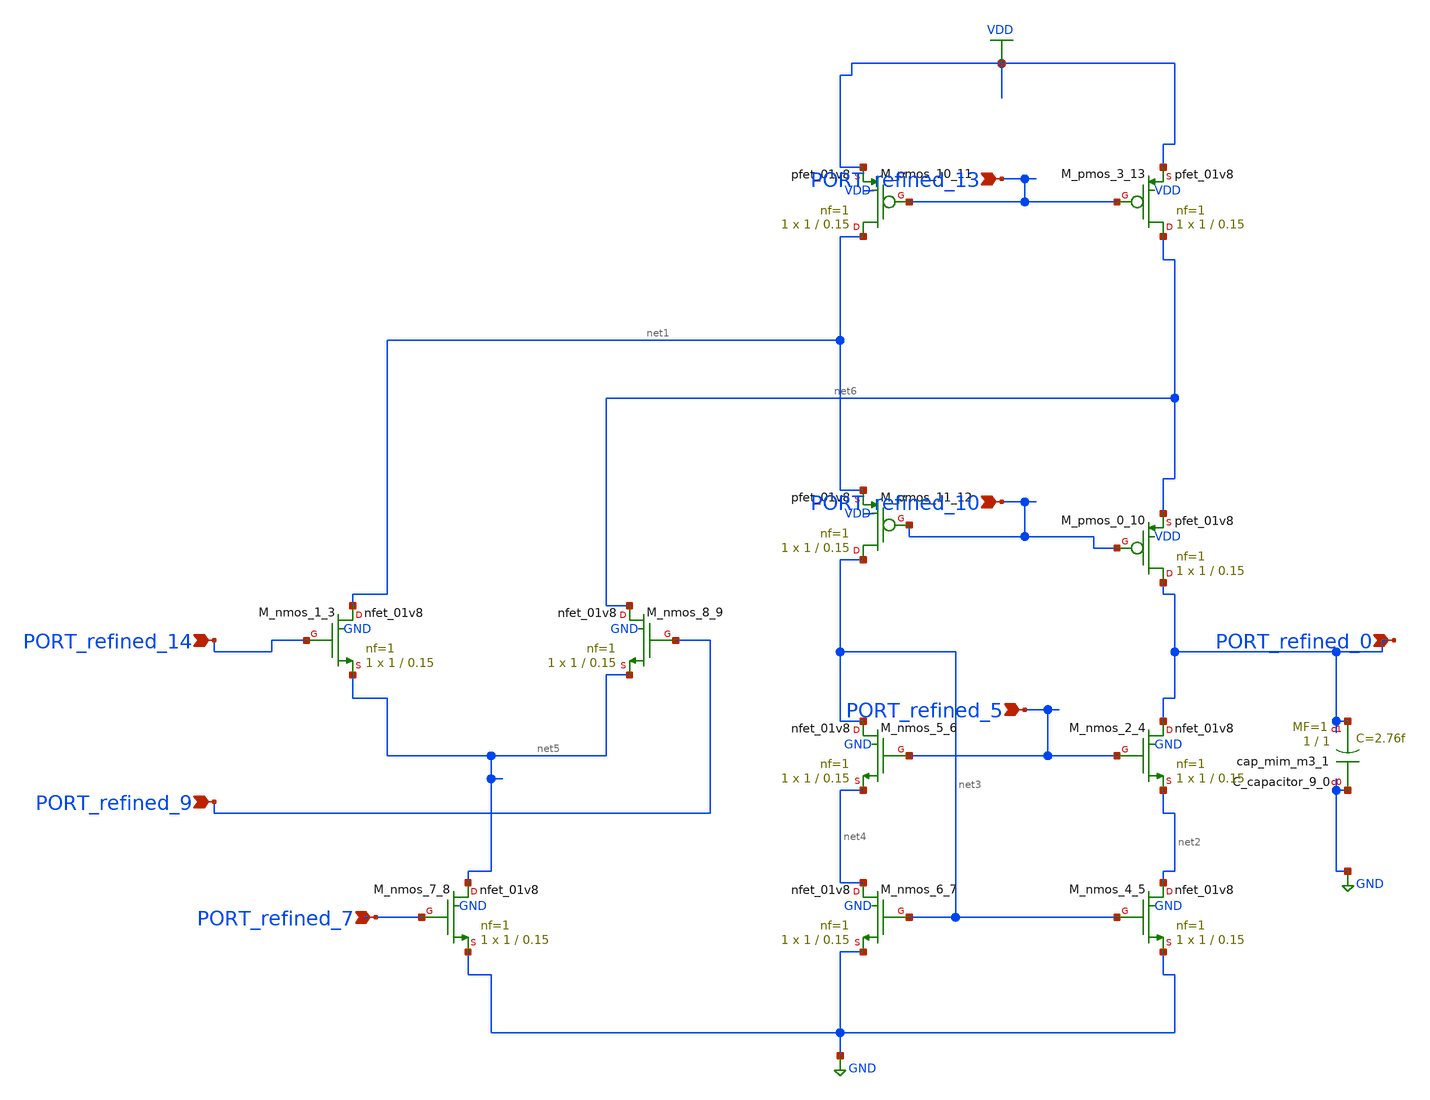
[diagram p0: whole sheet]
** sch_path: schematics/Image2Net/111.sch
**.subckt 111 PORT_refined_14 PORT_refined_0 PORT_refined_9 PORT_refined_7 PORT_refined_10
*+ PORT_refined_13 PORT_refined_5
*.ipin PORT_refined_14
*.ipin PORT_refined_0
*.ipin PORT_refined_9
*.ipin PORT_refined_7
*.ipin PORT_refined_10
*.ipin PORT_refined_13
*.ipin PORT_refined_5
XC_capacitor_9_0 GND PORT_refined_0 sky130_fd_pr__cap_mim_m3_1 W=1 L=1 MF=1 m=1
XM_nmos_1_3 net1 PORT_refined_14 net5 GND sky130_fd_pr__nfet_01v8 L=0.15 W=1 nf=1 ad='int((1 + 1)/2) * 1 / 1 * 0.29'
+ as='int((1 + 2)/2) * 1 / 1 * 0.29' pd='2*int((1 + 1)/2) * (1 / 1 + 0.29)' ps='2*int((1 + 2)/2) * (1 / 1 + 0.29)'
+ nrd='0.29 / 1 ' nrs='0.29 / 1 ' sa=0 sb=0 sd=0 mult=1 m=1
XM_nmos_2_4 PORT_refined_0 PORT_refined_5 net2 GND sky130_fd_pr__nfet_01v8 L=0.15 W=1 nf=1 ad='int((1 + 1)/2) * 1 / 1 * 0.29'
+ as='int((1 + 2)/2) * 1 / 1 * 0.29' pd='2*int((1 + 1)/2) * (1 / 1 + 0.29)' ps='2*int((1 + 2)/2) * (1 / 1 + 0.29)'
+ nrd='0.29 / 1 ' nrs='0.29 / 1 ' sa=0 sb=0 sd=0 mult=1 m=1
XM_nmos_4_5 net2 net3 GND GND sky130_fd_pr__nfet_01v8 L=0.15 W=1 nf=1 ad='int((1 + 1)/2) * 1 / 1 * 0.29'
+ as='int((1 + 2)/2) * 1 / 1 * 0.29' pd='2*int((1 + 1)/2) * (1 / 1 + 0.29)' ps='2*int((1 + 2)/2) * (1 / 1 + 0.29)'
+ nrd='0.29 / 1 ' nrs='0.29 / 1 ' sa=0 sb=0 sd=0 mult=1 m=1
XM_nmos_5_6 net3 PORT_refined_5 net4 GND sky130_fd_pr__nfet_01v8 L=0.15 W=1 nf=1 ad='int((1 + 1)/2) * 1 / 1 * 0.29'
+ as='int((1 + 2)/2) * 1 / 1 * 0.29' pd='2*int((1 + 1)/2) * (1 / 1 + 0.29)' ps='2*int((1 + 2)/2) * (1 / 1 + 0.29)'
+ nrd='0.29 / 1 ' nrs='0.29 / 1 ' sa=0 sb=0 sd=0 mult=1 m=1
XM_nmos_6_7 net4 net3 GND GND sky130_fd_pr__nfet_01v8 L=0.15 W=1 nf=1 ad='int((1 + 1)/2) * 1 / 1 * 0.29'
+ as='int((1 + 2)/2) * 1 / 1 * 0.29' pd='2*int((1 + 1)/2) * (1 / 1 + 0.29)' ps='2*int((1 + 2)/2) * (1 / 1 + 0.29)'
+ nrd='0.29 / 1 ' nrs='0.29 / 1 ' sa=0 sb=0 sd=0 mult=1 m=1
XM_nmos_7_8 net5 PORT_refined_7 GND GND sky130_fd_pr__nfet_01v8 L=0.15 W=1 nf=1 ad='int((1 + 1)/2) * 1 / 1 * 0.29'
+ as='int((1 + 2)/2) * 1 / 1 * 0.29' pd='2*int((1 + 1)/2) * (1 / 1 + 0.29)' ps='2*int((1 + 2)/2) * (1 / 1 + 0.29)'
+ nrd='0.29 / 1 ' nrs='0.29 / 1 ' sa=0 sb=0 sd=0 mult=1 m=1
XM_nmos_8_9 net6 PORT_refined_9 net5 GND sky130_fd_pr__nfet_01v8 L=0.15 W=1 nf=1 ad='int((1 + 1)/2) * 1 / 1 * 0.29'
+ as='int((1 + 2)/2) * 1 / 1 * 0.29' pd='2*int((1 + 1)/2) * (1 / 1 + 0.29)' ps='2*int((1 + 2)/2) * (1 / 1 + 0.29)'
+ nrd='0.29 / 1 ' nrs='0.29 / 1 ' sa=0 sb=0 sd=0 mult=1 m=1
XM_pmos_0_10 PORT_refined_0 PORT_refined_10 net6 VDD sky130_fd_pr__pfet_01v8 L=0.15 W=1 nf=1 ad='int((1 + 1)/2) * 1 / 1 * 0.29'
+ as='int((1 + 2)/2) * 1 / 1 * 0.29' pd='2*int((1 + 1)/2) * (1 / 1 + 0.29)' ps='2*int((1 + 2)/2) * (1 / 1 + 0.29)'
+ nrd='0.29 / 1 ' nrs='0.29 / 1 ' sa=0 sb=0 sd=0 mult=1 m=1
XM_pmos_10_11 net1 PORT_refined_13 VDD VDD sky130_fd_pr__pfet_01v8 L=0.15 W=1 nf=1 ad='int((1 + 1)/2) * 1 / 1 * 0.29'
+ as='int((1 + 2)/2) * 1 / 1 * 0.29' pd='2*int((1 + 1)/2) * (1 / 1 + 0.29)' ps='2*int((1 + 2)/2) * (1 / 1 + 0.29)'
+ nrd='0.29 / 1 ' nrs='0.29 / 1 ' sa=0 sb=0 sd=0 mult=1 m=1
XM_pmos_11_12 net3 PORT_refined_10 net1 VDD sky130_fd_pr__pfet_01v8 L=0.15 W=1 nf=1 ad='int((1 + 1)/2) * 1 / 1 * 0.29'
+ as='int((1 + 2)/2) * 1 / 1 * 0.29' pd='2*int((1 + 1)/2) * (1 / 1 + 0.29)' ps='2*int((1 + 2)/2) * (1 / 1 + 0.29)'
+ nrd='0.29 / 1 ' nrs='0.29 / 1 ' sa=0 sb=0 sd=0 mult=1 m=1
XM_pmos_3_13 net6 PORT_refined_13 VDD VDD sky130_fd_pr__pfet_01v8 L=0.15 W=1 nf=1 ad='int((1 + 1)/2) * 1 / 1 * 0.29'
+ as='int((1 + 2)/2) * 1 / 1 * 0.29' pd='2*int((1 + 1)/2) * (1 / 1 + 0.29)' ps='2*int((1 + 2)/2) * (1 / 1 + 0.29)'
+ nrd='0.29 / 1 ' nrs='0.29 / 1 ' sa=0 sb=0 sd=0 mult=1 m=1
**.ends
.GLOBAL GND
.GLOBAL VDD
.end
